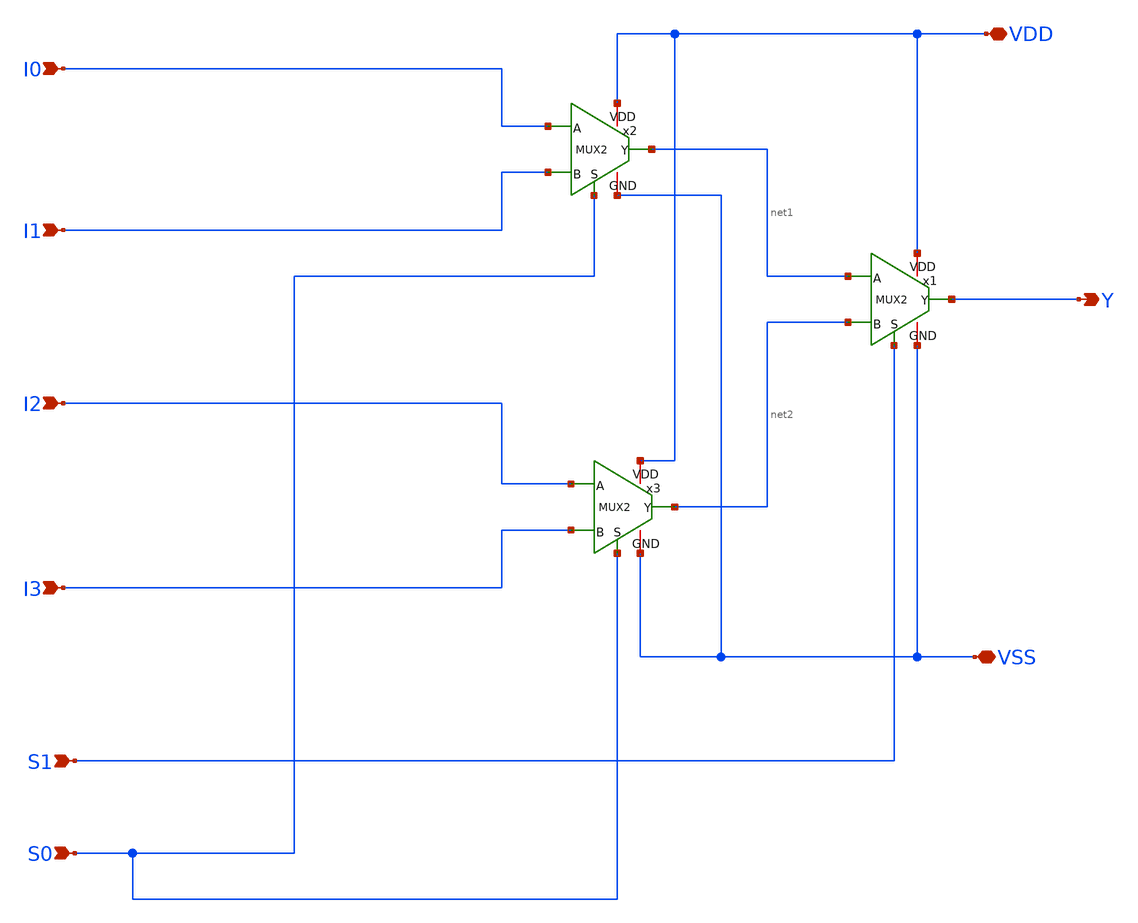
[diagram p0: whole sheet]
** sch_path: MUX/MUX4.sch
**.subckt MUX4 I3 I2 I1 I0 S0 S1 Y VDD VSS
*.ipin I3
*.ipin I2
*.ipin I1
*.ipin I0
*.ipin S0
*.ipin S1
*.opin Y
*.iopin VDD
*.iopin VSS
x1 net1 net2 S1 VDD Y VSS MUX2
x2 I0 I1 S0 VDD net1 VSS MUX2
x3 I2 I3 S0 VDD net2 VSS MUX2
**.ends

* expanding   symbol:  IP62_5_stdcell/MUX2.sym # of pins=6
** sym_path: IP62_5_stdcell/MUX2.sym
** sch_path: IP62_5_stdcell/MUX2.sch
.subckt MUX2 A B S VDD Y GND
*.ipin B
*.ipin S
*.opin Y
*.iopin VDD
*.iopin GND
*.ipin A
XM13 net1 S VDD VDD PMOS w=6.8u l=1u as=0 ad=0 ps=0 pd=0 nrd=0 nrs=0 m=1
XM9 net2 B VDD VDD PMOS w=6.8u l=1u as=0 ad=0 ps=0 pd=0 nrd=0 nrs=0 m=1
XM8 net4 net1 net2 VDD PMOS w=6.8u l=1u as=0 ad=0 ps=0 pd=0 nrd=0 nrs=0 m=1
XM10 Y net4 VDD VDD PMOS w=5.1u l=1u as=0 ad=0 ps=0 pd=0 nrd=0 nrs=0 m=2
XM2 net4 S net3 VDD PMOS w=6.8u l=1u as=0 ad=0 ps=0 pd=0 nrd=0 nrs=0 m=1
XM12 net1 S GND GND NMOS w=3.4u l=1u as=0 ad=0 ps=0 pd=0 nrd=0 nrs=0 m=1
XM3 net2 B GND GND NMOS w=3.4u l=1u as=0 ad=0 ps=0 pd=0 nrd=0 nrs=0 m=1
XM1 Y net4 GND GND NMOS w=3.4u l=1u as=0 ad=0 ps=0 pd=0 nrd=0 nrs=0 m=1
XM5 net3 A GND GND NMOS w=3.4u l=1u as=0 ad=0 ps=0 pd=0 nrd=0 nrs=0 m=1
XM6 net4 S net2 GND NMOS w=3.4u l=1u as=0 ad=0 ps=0 pd=0 nrd=0 nrs=0 m=2
XM4 net4 net1 net3 GND NMOS w=3.4u l=1u as=0 ad=0 ps=0 pd=0 nrd=0 nrs=0 m=2
XM7 net3 A VDD VDD PMOS w=6.8u l=1u as=0 ad=0 ps=0 pd=0 nrd=0 nrs=0 m=1
.ends

.end
